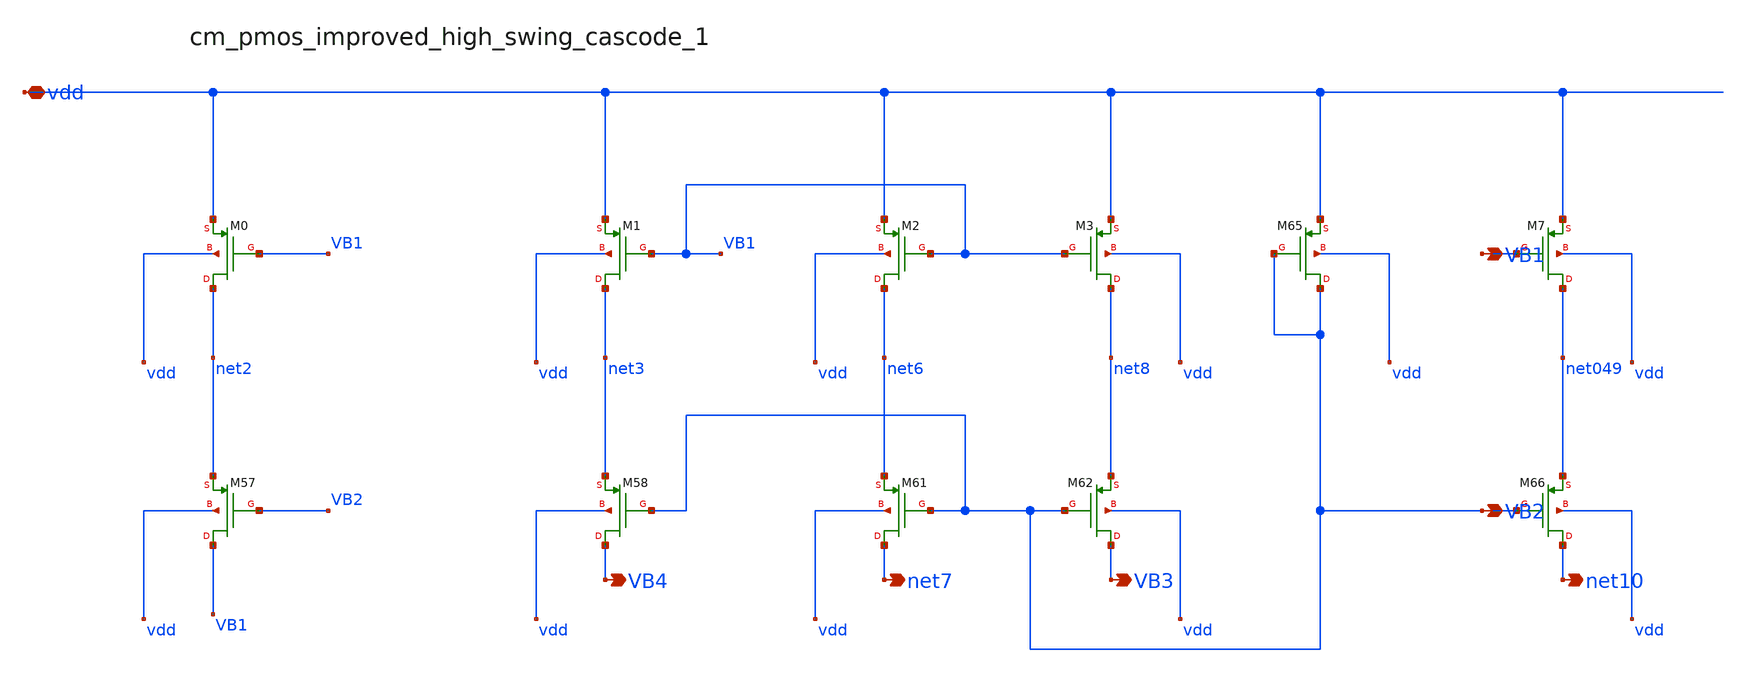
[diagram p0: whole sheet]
** sch_path: analog-db/raw/amp_011_peng_iac/hier/blocks/cm_pmos_improved_high_swing_cascode_1.sch
**.subckt cm_pmos_improved_high_swing_cascode_1 vdd VB1 VB2 VB4 net7 VB3 net10
*.iopin vdd
*.opin VB1
*.opin VB2
*.opin VB4
*.opin net7
*.opin VB3
*.opin net10
XM0 net2 VB1 vdd vdd sg13_lv_pmos w=x_dut_xm0_w l=x_dut_xm0_l ng=1 m=x_dut_xm0_m
XM1 net3 VB1 vdd vdd sg13_lv_pmos w=x_dut_xm1_w l=x_dut_xm1_l ng=1 m=x_dut_xm1_m
XM2 net6 VB1 vdd vdd sg13_lv_pmos w=x_dut_xm2_w l=x_dut_xm2_l ng=1 m=x_dut_xm2_m
XM3 net8 VB1 vdd vdd sg13_lv_pmos w=x_dut_xm3_w l=x_dut_xm3_l ng=1 m=x_dut_xm3_m
XM57 VB1 VB2 net2 vdd sg13_lv_pmos w=x_dut_xm57_w l=x_dut_xm57_l ng=1 m=x_dut_xm57_m
XM58 VB4 VB2 net3 vdd sg13_lv_pmos w=x_dut_xm58_w l=x_dut_xm58_l ng=1 m=x_dut_xm58_m
XM61 net7 VB2 net6 vdd sg13_lv_pmos w=x_dut_xm61_w l=x_dut_xm61_l ng=1 m=x_dut_xm61_m
XM62 VB3 VB2 net8 vdd sg13_lv_pmos w=x_dut_xm62_w l=x_dut_xm62_l ng=1 m=x_dut_xm62_m
XM65 VB2 VB2 vdd vdd sg13_lv_pmos w=x_dut_xm65_w l=x_dut_xm65_l ng=1 m=x_dut_xm65_m
XM66 net10 VB2 net049 vdd sg13_lv_pmos w=x_dut_xm66_w l=x_dut_xm66_l ng=1 m=x_dut_xm66_m
XM7 net049 VB1 vdd vdd sg13_lv_pmos w=x_dut_xm7_w l=x_dut_xm7_l ng=1 m=x_dut_xm7_m
**.ends
.end
